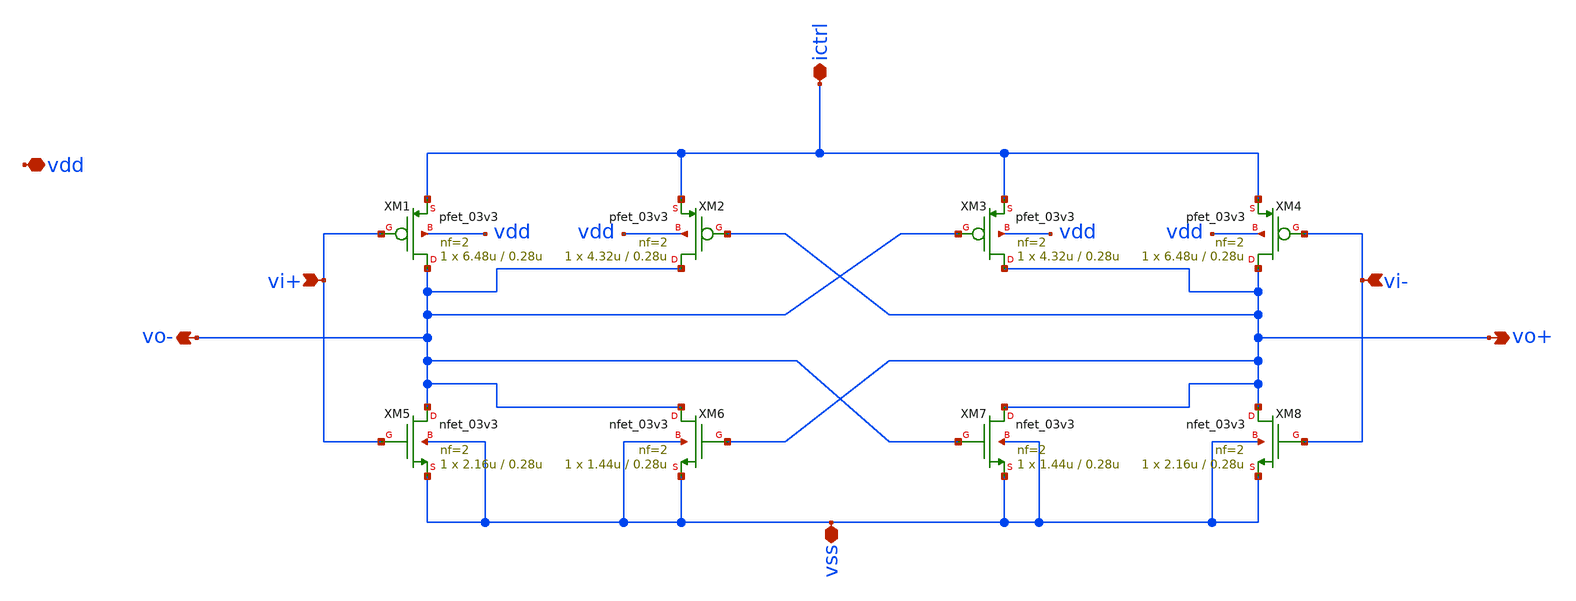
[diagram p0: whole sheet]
** sch_path: xschem/single_delay.sch
**.subckt single_delay ictrl vss vdd vi+ vi- vo- vo+
*.iopin ictrl
*.iopin vss
*.iopin vdd
*.ipin vi+
*.ipin vi-
*.opin vo-
*.opin vo+
XM1 vo- vi+ ictrl vdd pfet_03v3 L=0.28u W=6.48u nf=2 ad='int((nf+1)/2) * W/nf * 0.18u' as='int((nf+2)/2) * W/nf * 0.18u'
+ pd='2*int((nf+1)/2) * (W/nf + 0.18u)' ps='2*int((nf+2)/2) * (W/nf + 0.18u)' nrd='0.18u / W' nrs='0.18u / W'
+ sa=0 sb=0 sd=0 m=1
XM2 vo- vo+ ictrl vdd pfet_03v3 L=0.28u W=4.32u nf=2 ad='int((nf+1)/2) * W/nf * 0.18u' as='int((nf+2)/2) * W/nf * 0.18u'
+ pd='2*int((nf+1)/2) * (W/nf + 0.18u)' ps='2*int((nf+2)/2) * (W/nf + 0.18u)' nrd='0.18u / W' nrs='0.18u / W'
+ sa=0 sb=0 sd=0 m=1
XM3 vo+ vo- ictrl vdd pfet_03v3 L=0.28u W=4.32u nf=2 ad='int((nf+1)/2) * W/nf * 0.18u' as='int((nf+2)/2) * W/nf * 0.18u'
+ pd='2*int((nf+1)/2) * (W/nf + 0.18u)' ps='2*int((nf+2)/2) * (W/nf + 0.18u)' nrd='0.18u / W' nrs='0.18u / W'
+ sa=0 sb=0 sd=0 m=1
XM4 vo+ vi- ictrl vdd pfet_03v3 L=0.28u W=6.48u nf=2 ad='int((nf+1)/2) * W/nf * 0.18u' as='int((nf+2)/2) * W/nf * 0.18u'
+ pd='2*int((nf+1)/2) * (W/nf + 0.18u)' ps='2*int((nf+2)/2) * (W/nf + 0.18u)' nrd='0.18u / W' nrs='0.18u / W'
+ sa=0 sb=0 sd=0 m=1
XM5 vo- vi+ vss vss nfet_03v3 L=0.28u W=2.16u nf=2 ad='int((nf+1)/2) * W/nf * 0.18u' as='int((nf+2)/2) * W/nf * 0.18u'
+ pd='2*int((nf+1)/2) * (W/nf + 0.18u)' ps='2*int((nf+2)/2) * (W/nf + 0.18u)' nrd='0.18u / W' nrs='0.18u / W'
+ sa=0 sb=0 sd=0 m=1
XM6 vo- vo+ vss vss nfet_03v3 L=0.28u W=1.44u nf=2 ad='int((nf+1)/2) * W/nf * 0.18u' as='int((nf+2)/2) * W/nf * 0.18u'
+ pd='2*int((nf+1)/2) * (W/nf + 0.18u)' ps='2*int((nf+2)/2) * (W/nf + 0.18u)' nrd='0.18u / W' nrs='0.18u / W'
+ sa=0 sb=0 sd=0 m=1
XM7 vo+ vo- vss vss nfet_03v3 L=0.28u W=1.44u nf=2 ad='int((nf+1)/2) * W/nf * 0.18u' as='int((nf+2)/2) * W/nf * 0.18u'
+ pd='2*int((nf+1)/2) * (W/nf + 0.18u)' ps='2*int((nf+2)/2) * (W/nf + 0.18u)' nrd='0.18u / W' nrs='0.18u / W'
+ sa=0 sb=0 sd=0 m=1
XM8 vo+ vi- vss vss nfet_03v3 L=0.28u W=2.16u nf=2 ad='int((nf+1)/2) * W/nf * 0.18u' as='int((nf+2)/2) * W/nf * 0.18u'
+ pd='2*int((nf+1)/2) * (W/nf + 0.18u)' ps='2*int((nf+2)/2) * (W/nf + 0.18u)' nrd='0.18u / W' nrs='0.18u / W'
+ sa=0 sb=0 sd=0 m=1
**.ends
.end
